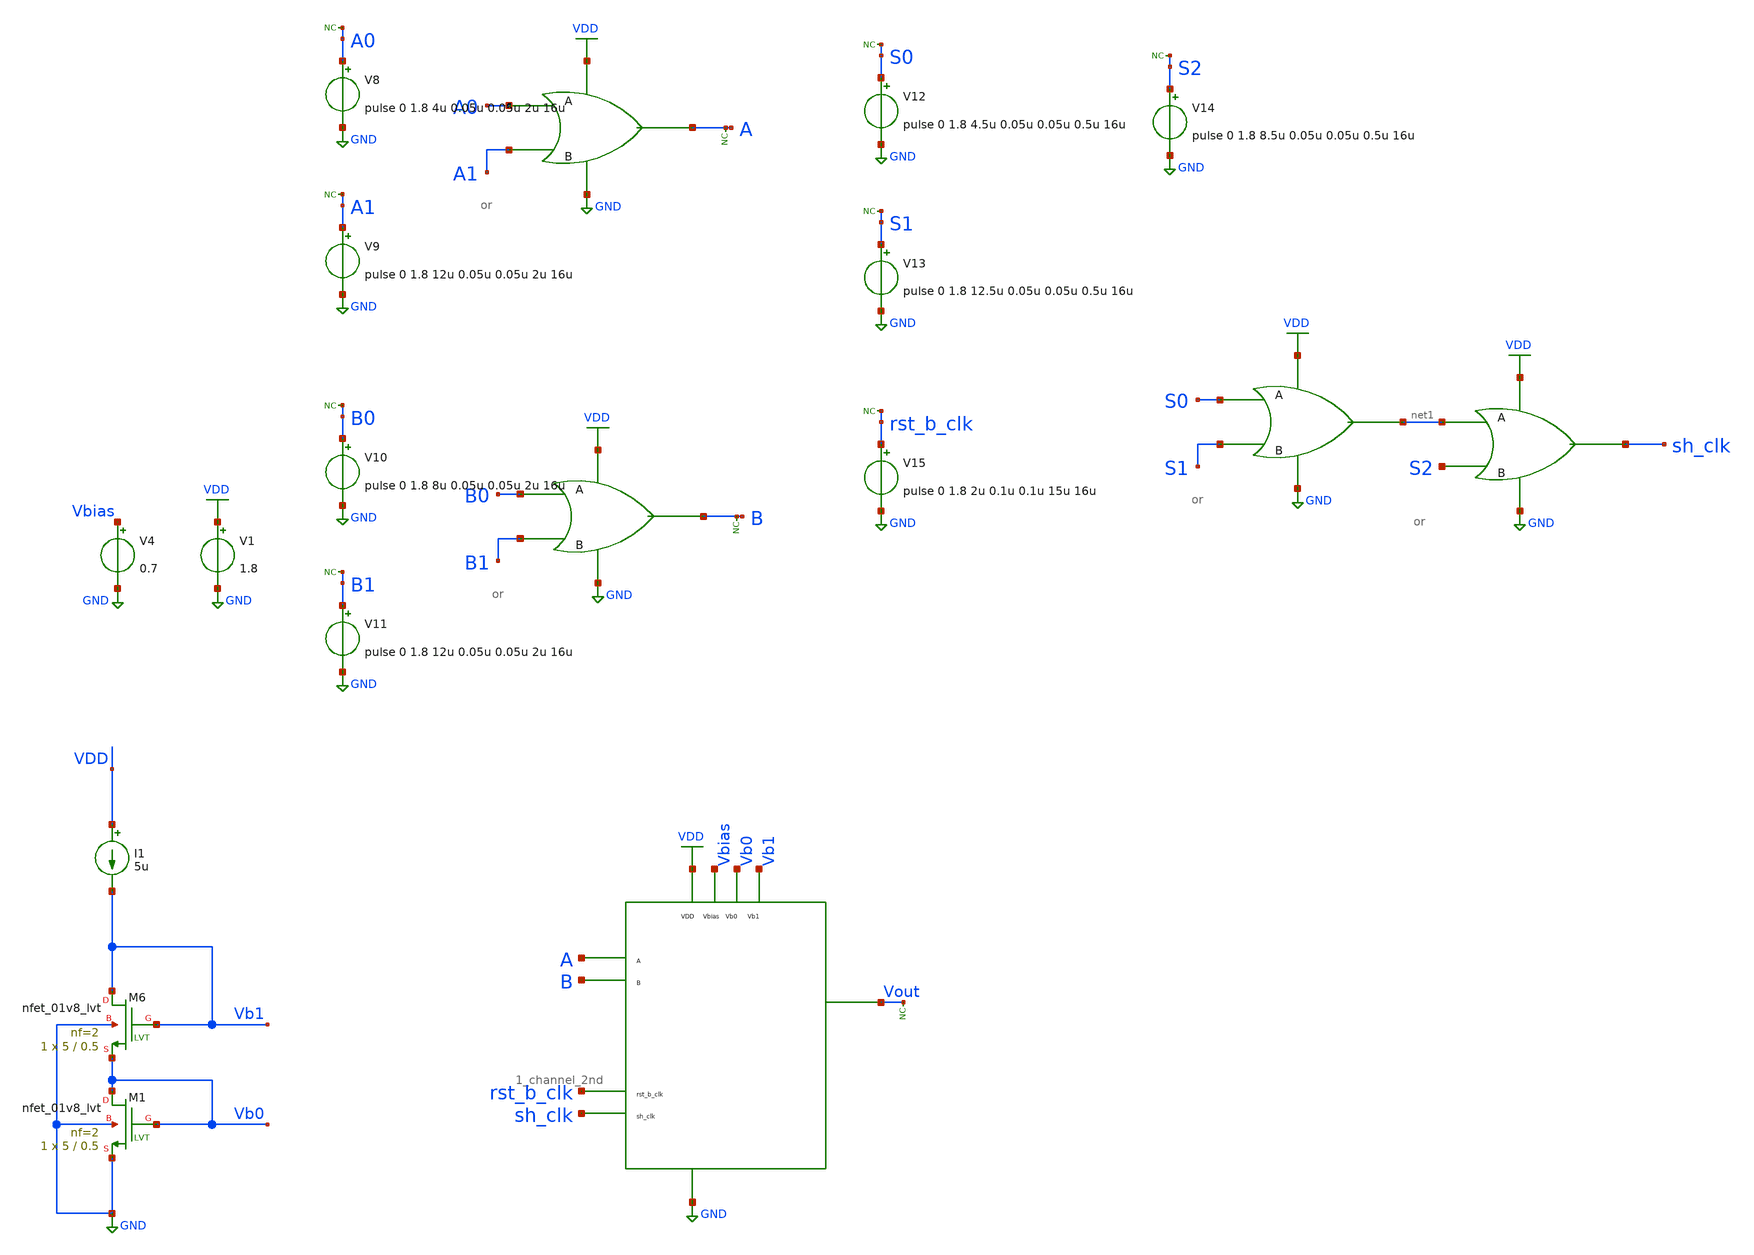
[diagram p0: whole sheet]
** sch_path: xschem/cmos_imager/tb_1_channel_rc.sch
**.subckt tb_1_channel_rc
XM6 Vb1 Vb1 Vb0 GND sky130_fd_pr__nfet_01v8_lvt L=0.5 W=5 nf=2 ad='int((nf+1)/2) * W/nf * 0.29' as='int((nf+2)/2) * W/nf * 0.29'
+ pd='2*int((nf+1)/2) * (W/nf + 0.29)' ps='2*int((nf+2)/2) * (W/nf + 0.29)' nrd='0.29 / W' nrs='0.29 / W'
+ sa=0 sb=0 sd=0 mult=1 m=1
XM1 Vb0 Vb0 GND GND sky130_fd_pr__nfet_01v8_lvt L=0.5 W=5 nf=2 ad='int((nf+1)/2) * W/nf * 0.29' as='int((nf+2)/2) * W/nf * 0.29'
+ pd='2*int((nf+1)/2) * (W/nf + 0.29)' ps='2*int((nf+2)/2) * (W/nf + 0.29)' nrd='0.29 / W' nrs='0.29 / W'
+ sa=0 sb=0 sd=0 mult=1 m=1
I1 VDD Vb1 5u
V1 VDD GND 1.8
V4 Vbias GND 0.7
X10 A0 A GND VDD A1 or
* noconn A
X11 B0 B GND VDD B1 or
* noconn B
V8 A0 GND pulse 0 1.8 4u 0.05u 0.05u 2u 16u
* noconn A0
V9 A1 GND pulse 0 1.8 12u 0.05u 0.05u 2u 16u
* noconn A1
V10 B0 GND pulse 0 1.8 8u 0.05u 0.05u 2u 16u
* noconn B0
V11 B1 GND pulse 0 1.8 12u 0.05u 0.05u 2u 16u
* noconn B1
V12 S0 GND pulse 0 1.8 4.5u 0.05u 0.05u 0.5u 16u
* noconn S0
V13 S1 GND pulse 0 1.8 12.5u 0.05u 0.05u 0.5u 16u
* noconn S1
V14 S2 GND pulse 0 1.8 8.5u 0.05u 0.05u 0.5u 16u
* noconn S2
X12 S0 net1 GND VDD S1 or
X13 net1 sh_clk GND VDD S2 or
V15 rst_b_clk GND pulse 0 1.8 2u 0.1u 0.1u 15u 16u
* noconn rst_b_clk
X14 A GND VDD B Vbias Vout Vb0 Vb1 rst_b_clk sh_clk 1_channel_2nd
* noconn Vout
**** begin user architecture code

** opencircuitdesign pdks install
.lib $::SKYWATER_MODELS/sky130.lib.spice tt




*.dc Vdd 0 2 0.1
.option temp=37
.control
save all
run
tran 0.1n 50u
display

*plot Vin_1 Vin_2 Vin_3 Vpixel_out
*plot Vpixel_out Vbuff_out Vcap Vout
plot A B sh_clk rst_b_clk
plot Vout
*plot rst_b_clk sh_clk
*plot sh_clk sh_clk_b
*plot Vcap Vout
*plot vm1#branch
*plot vm2#branch
*plot vm3#branch

.endc


**** end user architecture code
**.ends
.GLOBAL GND
.GLOBAL VDD
.end
